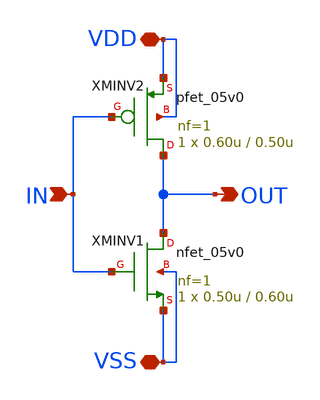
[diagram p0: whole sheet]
** sch_path: designs/libs/core_biasgen/biasgen_inverter/biasgen_inverter.sch
**.subckt biasgen_inverter VDD VSS IN OUT
*.iopin VDD
*.iopin VSS
*.ipin IN
*.opin OUT
XMINV1 OUT IN VSS VSS nfet_05v0 L=0.60u W=0.50u nf=1 ad='int((nf+1)/2) * W/nf * 0.18u' as='int((nf+2)/2) * W/nf * 0.18u'
+ pd='2*int((nf+1)/2) * (W/nf + 0.18u)' ps='2*int((nf+2)/2) * (W/nf + 0.18u)' nrd='0.18u / W' nrs='0.18u / W'
+ sa=0 sb=0 sd=0 m=1
XMINV2 OUT IN VDD VDD pfet_05v0 L=0.50u W=0.60u nf=1 ad='int((nf+1)/2) * W/nf * 0.18u' as='int((nf+2)/2) * W/nf * 0.18u'
+ pd='2*int((nf+1)/2) * (W/nf + 0.18u)' ps='2*int((nf+2)/2) * (W/nf + 0.18u)' nrd='0.18u / W' nrs='0.18u / W'
+ sa=0 sb=0 sd=0 m=1
**.ends
.end
